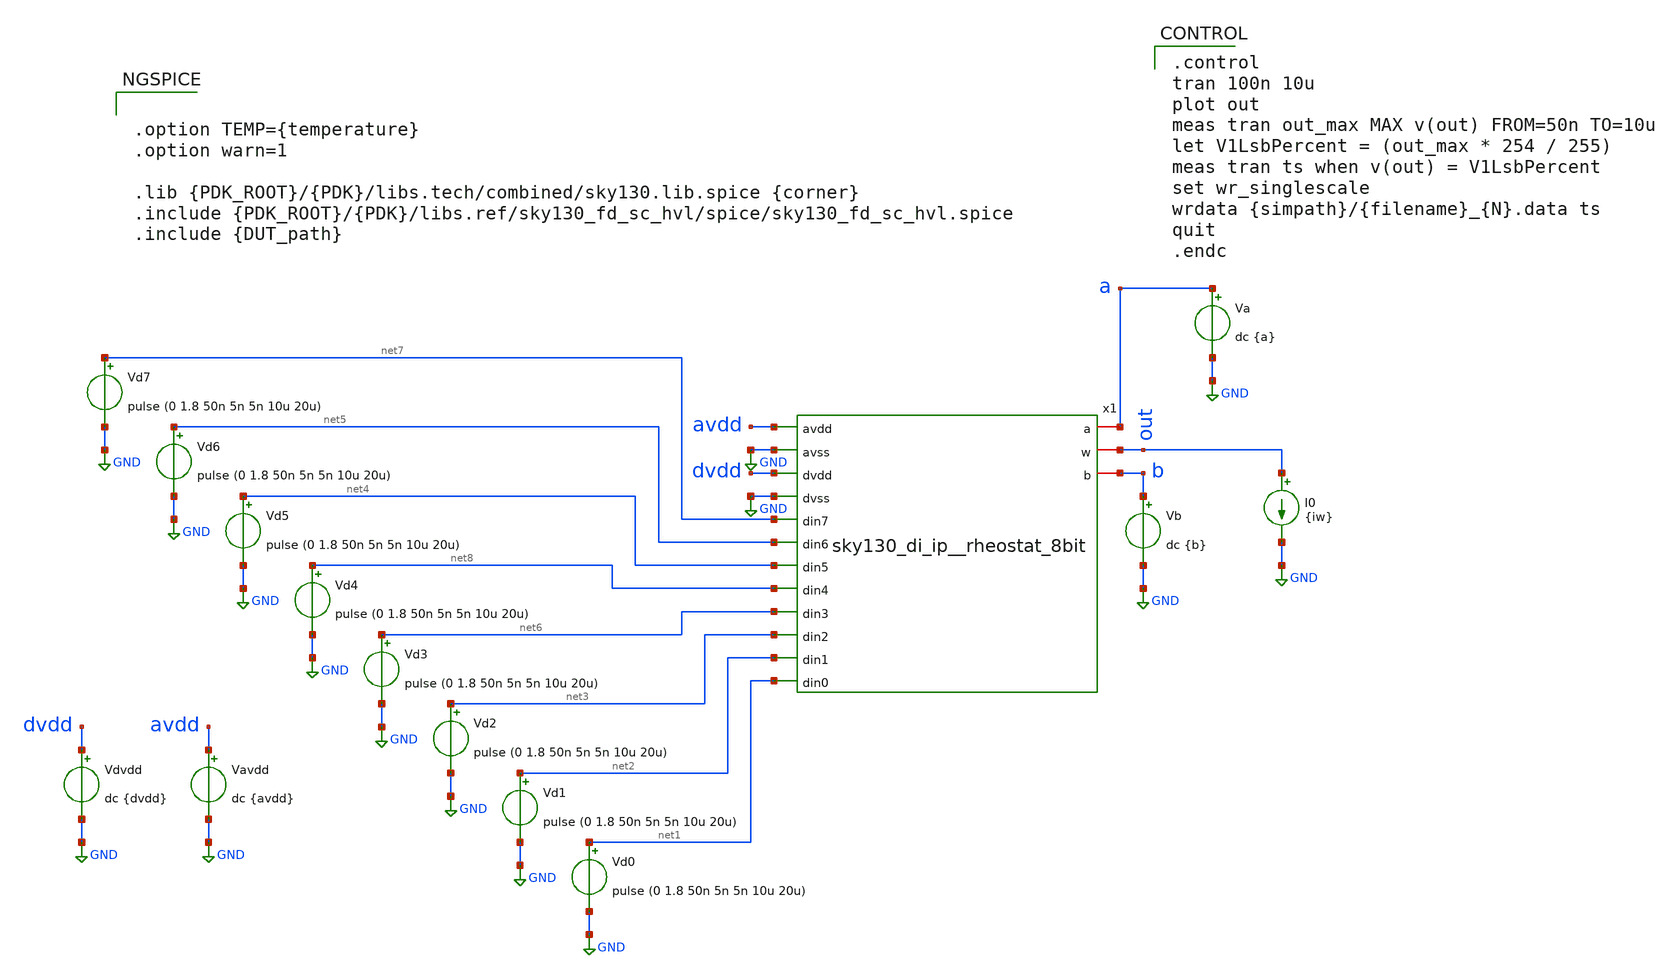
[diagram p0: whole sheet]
** sch_path: cace/tb_tran.sch
**.subckt tb_tran
x1 avdd GND dvdd GND net7 net5 net4 a net8 net6 out net3 net2 net1 b sky130_di_ip__rheostat_8bit
Vd0 net1 GND pulse (0 1.8 50n 5n 5n 10u 20u)
Vd1 net2 GND pulse (0 1.8 50n 5n 5n 10u 20u)
Vd2 net3 GND pulse (0 1.8 50n 5n 5n 10u 20u)
Vd3 net6 GND pulse (0 1.8 50n 5n 5n 10u 20u)
Vd4 net8 GND pulse (0 1.8 50n 5n 5n 10u 20u)
Vd5 net4 GND pulse (0 1.8 50n 5n 5n 10u 20u)
Vd6 net5 GND pulse (0 1.8 50n 5n 5n 10u 20u)
Vd7 net7 GND pulse (0 1.8 50n 5n 5n 10u 20u)
Vdvdd dvdd GND dc {dvdd}
Vavdd avdd GND dc {avdd}
Va a GND dc {a}
Vb b GND dc {b}
I0 out GND {iw}
**** begin user architecture code


.option TEMP={temperature}
.option warn=1

.lib {PDK_ROOT}/{PDK}/libs.tech/combined/sky130.lib.spice {corner}
.include {PDK_ROOT}/{PDK}/libs.ref/sky130_fd_sc_hvl/spice/sky130_fd_sc_hvl.spice
.include {DUT_path}



.control
tran 100n 10u
plot out
meas tran out_max MAX v(out) FROM=50n TO=10u
let V1LsbPercent = (out_max * 254 / 255)
meas tran ts when v(out) = V1LsbPercent
set wr_singlescale
wrdata {simpath}/{filename}_{N}.data ts
quit
.endc




.subckt sky130_fd_sc_hvl__inv_1 A VGND VNB VPB VPWR Y
X0 VPWR A Y VPB sky130_fd_pr__pfet_g5v0d10v5 w=1.5e+06u l=500000u
X1 VGND A Y VNB sky130_fd_pr__nfet_g5v0d10v5 w=750000u l=500000u
.ends

.subckt sky130_fd_sc_hvl__lsbuflv2hv_1 A LVPWR VGND VNB VPB VPWR X
X0 VGND a_404_1133# a_504_1221# VNB sky130_fd_pr__nfet_g5v0d10v5 w=1.5e+06u l=500000u
X1 a_504_1221# a_404_1133# VGND VNB sky130_fd_pr__nfet_g5v0d10v5 w=1.5e+06u l=500000u
X2 X a_1711_885# VPWR VPB sky130_fd_pr__pfet_g5v0d10v5 w=1.5e+06u l=500000u
X3 X a_1711_885# VGND VNB sky130_fd_pr__nfet_g5v0d10v5 w=750000u l=500000u
X4 VGND A a_404_1133# VNB sky130_fd_pr__nfet_01v8 w=840000u l=150000u
X5 a_1197_107# a_772_151# VGND VNB sky130_fd_pr__nfet_g5v0d10v5 w=1.5e+06u l=500000u
X6 VPWR a_1197_107# a_504_1221# VPB sky130_fd_pr__pfet_g5v0d10v5 w=420000u l=1e+06u
X7 a_504_1221# a_404_1133# VGND VNB sky130_fd_pr__nfet_g5v0d10v5 w=1.5e+06u l=500000u
X8 a_1197_107# a_772_151# VGND VNB sky130_fd_pr__nfet_g5v0d10v5 w=1.5e+06u l=500000u
X9 a_772_151# a_404_1133# VGND VNB sky130_fd_pr__nfet_01v8 w=840000u l=150000u
X10 a_504_1221# a_404_1133# VGND VNB sky130_fd_pr__nfet_g5v0d10v5 w=1.5e+06u l=500000u
X11 VGND a_404_1133# a_504_1221# VNB sky130_fd_pr__nfet_g5v0d10v5 w=1.5e+06u l=500000u
X12 LVPWR A a_404_1133# LVPWR sky130_fd_pr__pfet_01v8_hvt w=840000u l=150000u
X13 VGND a_772_151# a_1197_107# VNB sky130_fd_pr__nfet_g5v0d10v5 w=1.5e+06u l=500000u
X14 VPWR a_504_1221# a_1711_885# VPB sky130_fd_pr__pfet_g5v0d10v5 w=1.5e+06u l=500000u
X15 VGND a_504_1221# a_1711_885# VNB sky130_fd_pr__nfet_g5v0d10v5 w=750000u l=500000u
X16 VGND a_772_151# a_1197_107# VNB sky130_fd_pr__nfet_g5v0d10v5 w=1.5e+06u l=500000u
X17 a_772_151# a_404_1133# LVPWR LVPWR sky130_fd_pr__pfet_01v8_hvt w=840000u l=150000u
X18 a_1197_107# a_772_151# VGND VNB sky130_fd_pr__nfet_g5v0d10v5 w=1.5e+06u l=500000u
X19 VPWR a_504_1221# a_1197_107# VPB sky130_fd_pr__pfet_g5v0d10v5 w=420000u l=1e+06u
.ends


**** end user architecture code
**.ends
.GLOBAL GND
.end
